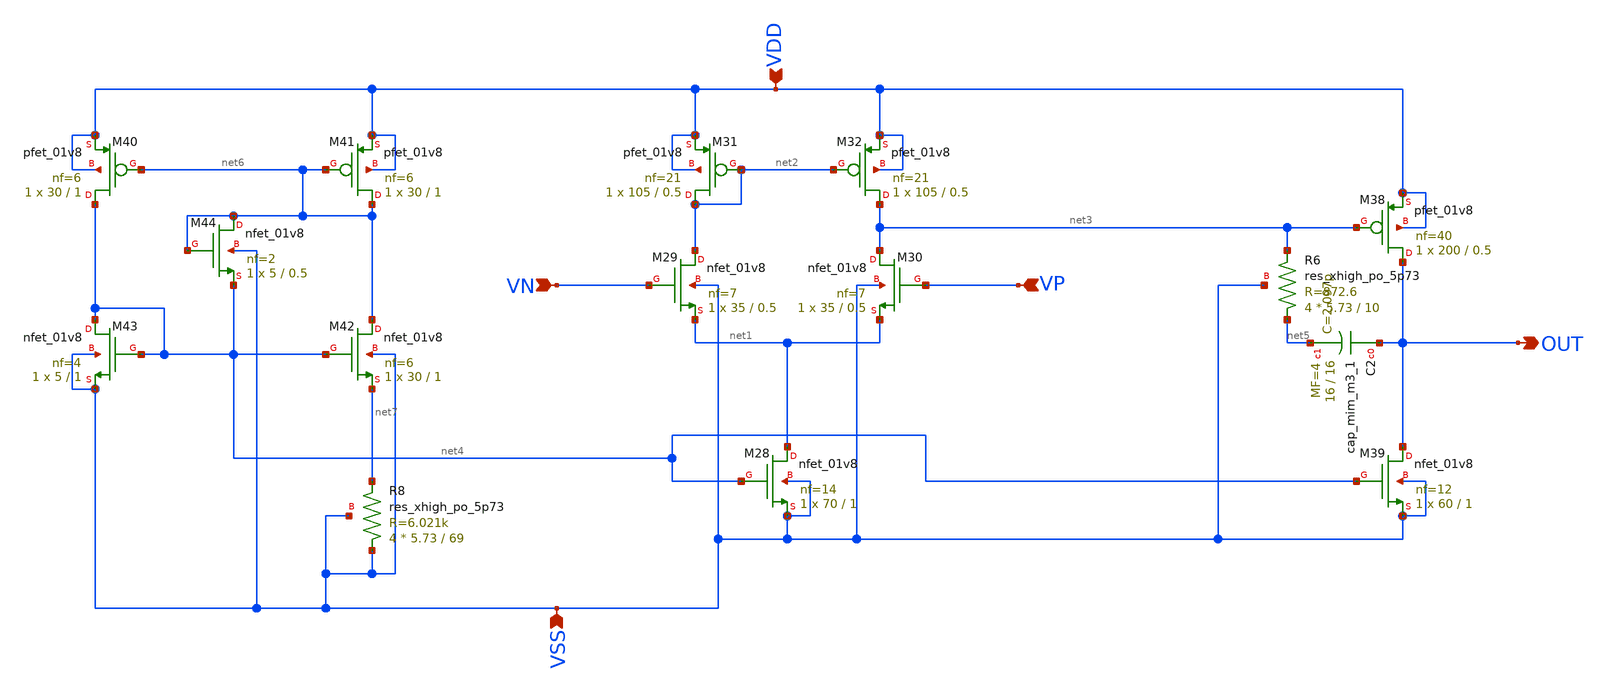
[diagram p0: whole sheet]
** sch_path: SP24_caravel_user_project_analog/xschem/xschem_DeltaSigma/C2S2_Amp_F_I.sch
**.subckt C2S2_Amp_F_I VN VDD VSS VP OUT
*.ipin VN
*.ipin VDD
*.ipin VSS
*.ipin VP
*.opin OUT
XM28 net1 net4 VSS VSS sky130_fd_pr__nfet_01v8 L=1 W=70 nf=14 ad='int((nf+1)/2) * W/nf * 0.29' as='int((nf+2)/2) * W/nf * 0.29'
+ pd='2*int((nf+1)/2) * (W/nf + 0.29)' ps='2*int((nf+2)/2) * (W/nf + 0.29)' nrd='0.29 / W' nrs='0.29 / W'
+ sa=0 sb=0 sd=0 mult=1 m=1
XM29 net2 VN net1 VSS sky130_fd_pr__nfet_01v8 L=0.5 W=35 nf=7 ad='int((nf+1)/2) * W/nf * 0.29' as='int((nf+2)/2) * W/nf * 0.29'
+ pd='2*int((nf+1)/2) * (W/nf + 0.29)' ps='2*int((nf+2)/2) * (W/nf + 0.29)' nrd='0.29 / W' nrs='0.29 / W'
+ sa=0 sb=0 sd=0 mult=1 m=1
XM30 net3 VP net1 VSS sky130_fd_pr__nfet_01v8 L=0.5 W=35 nf=7 ad='int((nf+1)/2) * W/nf * 0.29' as='int((nf+2)/2) * W/nf * 0.29'
+ pd='2*int((nf+1)/2) * (W/nf + 0.29)' ps='2*int((nf+2)/2) * (W/nf + 0.29)' nrd='0.29 / W' nrs='0.29 / W'
+ sa=0 sb=0 sd=0 mult=1 m=1
XM31 net2 net2 VDD VDD sky130_fd_pr__pfet_01v8 L=0.5 W=105 nf=21 ad='int((nf+1)/2) * W/nf * 0.29' as='int((nf+2)/2) * W/nf * 0.29'
+ pd='2*int((nf+1)/2) * (W/nf + 0.29)' ps='2*int((nf+2)/2) * (W/nf + 0.29)' nrd='0.29 / W' nrs='0.29 / W'
+ sa=0 sb=0 sd=0 mult=1 m=1
XM32 net3 net2 VDD VDD sky130_fd_pr__pfet_01v8 L=0.5 W=105 nf=21 ad='int((nf+1)/2) * W/nf * 0.29' as='int((nf+2)/2) * W/nf * 0.29'
+ pd='2*int((nf+1)/2) * (W/nf + 0.29)' ps='2*int((nf+2)/2) * (W/nf + 0.29)' nrd='0.29 / W' nrs='0.29 / W'
+ sa=0 sb=0 sd=0 mult=1 m=1
XM38 OUT net3 VDD VDD sky130_fd_pr__pfet_01v8 L=0.5 W=200 nf=40 ad='int((nf+1)/2) * W/nf * 0.29' as='int((nf+2)/2) * W/nf * 0.29'
+ pd='2*int((nf+1)/2) * (W/nf + 0.29)' ps='2*int((nf+2)/2) * (W/nf + 0.29)' nrd='0.29 / W' nrs='0.29 / W'
+ sa=0 sb=0 sd=0 mult=1 m=1
XM39 OUT net4 VSS VSS sky130_fd_pr__nfet_01v8 L=1 W=60 nf=12 ad='int((nf+1)/2) * W/nf * 0.29' as='int((nf+2)/2) * W/nf * 0.29'
+ pd='2*int((nf+1)/2) * (W/nf + 0.29)' ps='2*int((nf+2)/2) * (W/nf + 0.29)' nrd='0.29 / W' nrs='0.29 / W'
+ sa=0 sb=0 sd=0 mult=1 m=1
XC2 OUT net5 sky130_fd_pr__cap_mim_m3_1 W=16 L=16 MF=4 m=4
XR6 net5 net3 VSS sky130_fd_pr__res_xhigh_po_5p73 L=10 mult=4 m=4
XM40 net4 net6 VDD VDD sky130_fd_pr__pfet_01v8 L=1 W=30 nf=6 ad='int((nf+1)/2) * W/nf * 0.29' as='int((nf+2)/2) * W/nf * 0.29'
+ pd='2*int((nf+1)/2) * (W/nf + 0.29)' ps='2*int((nf+2)/2) * (W/nf + 0.29)' nrd='0.29 / W' nrs='0.29 / W'
+ sa=0 sb=0 sd=0 mult=1 m=1
XM41 net6 net6 VDD VDD sky130_fd_pr__pfet_01v8 L=1 W=30 nf=6 ad='int((nf+1)/2) * W/nf * 0.29' as='int((nf+2)/2) * W/nf * 0.29'
+ pd='2*int((nf+1)/2) * (W/nf + 0.29)' ps='2*int((nf+2)/2) * (W/nf + 0.29)' nrd='0.29 / W' nrs='0.29 / W'
+ sa=0 sb=0 sd=0 mult=1 m=1
XM42 net6 net4 net7 VSS sky130_fd_pr__nfet_01v8 L=1 W=30 nf=6 ad='int((nf+1)/2) * W/nf * 0.29' as='int((nf+2)/2) * W/nf * 0.29'
+ pd='2*int((nf+1)/2) * (W/nf + 0.29)' ps='2*int((nf+2)/2) * (W/nf + 0.29)' nrd='0.29 / W' nrs='0.29 / W'
+ sa=0 sb=0 sd=0 mult=1 m=1
XM43 net4 net4 VSS VSS sky130_fd_pr__nfet_01v8 L=1 W=5 nf=4 ad='int((nf+1)/2) * W/nf * 0.29' as='int((nf+2)/2) * W/nf * 0.29'
+ pd='2*int((nf+1)/2) * (W/nf + 0.29)' ps='2*int((nf+2)/2) * (W/nf + 0.29)' nrd='0.29 / W' nrs='0.29 / W'
+ sa=0 sb=0 sd=0 mult=1 m=1
XM44 net6 net6 net4 VSS sky130_fd_pr__nfet_01v8 L=0.5 W=5 nf=2 ad='int((nf+1)/2) * W/nf * 0.29' as='int((nf+2)/2) * W/nf * 0.29'
+ pd='2*int((nf+1)/2) * (W/nf + 0.29)' ps='2*int((nf+2)/2) * (W/nf + 0.29)' nrd='0.29 / W' nrs='0.29 / W'
+ sa=0 sb=0 sd=0 mult=1 m=1
XR8 VSS net7 VSS sky130_fd_pr__res_xhigh_po_5p73 L=69 mult=4 m=4
**.ends
.end
